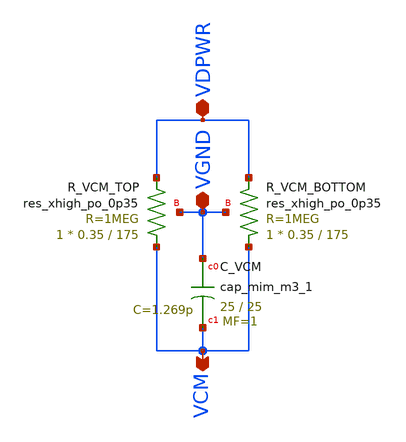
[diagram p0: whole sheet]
** sch_path: xschem/vcm_gen.sch
**.subckt vcm_gen VGND VDPWR VCM
*.iopin VGND
*.iopin VDPWR
*.opin VCM
XC_VCM VGND VCM sky130_fd_pr__cap_mim_m3_1 W=25 L=25 MF=1 m=1
XR_VCM_TOP VCM VDPWR VGND sky130_fd_pr__res_xhigh_po_0p35 L=175 mult=1 m=1
XR_VCM_BOTTOM VCM VDPWR VGND sky130_fd_pr__res_xhigh_po_0p35 L=175 mult=1 m=1
**.ends
.end
